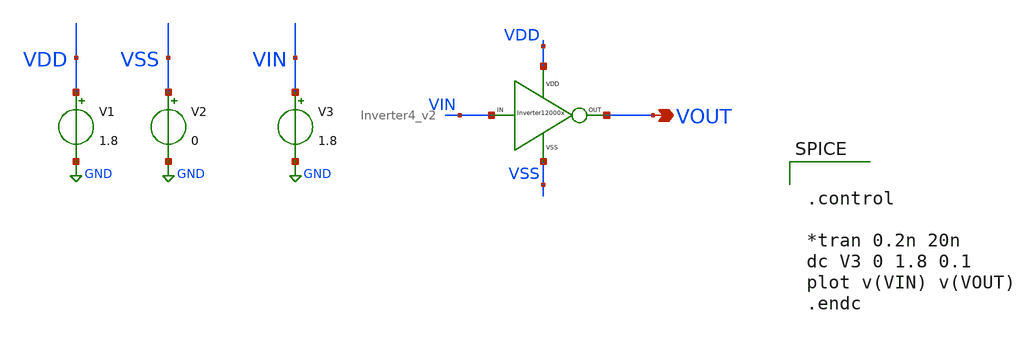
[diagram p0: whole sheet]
** sch_path: xschem/DC_DC_Converter_xschem/OTHERS/DC_DC_Converter_JV9/Inverter_4_v2/Inverter4_v2_TB.sch
**.subckt Inverter4_v2_TB VOUT
*.opin VOUT
V1 VDD GND 1.8
V2 VSS GND 0
V3 VIN GND 1.8
X1 VIN VDD VSS VOUT Inverter4_v2
**** begin user architecture code


.control

*tran 0.2n 20n
dc V3 0 1.8 0.1
plot v(VIN) v(VOUT)
.endc



** opencircuitdesign pdks install
.lib $::SKYWATER_MODELS/sky130.lib.spice tt


**** end user architecture code
**.ends
.GLOBAL GND
.end
